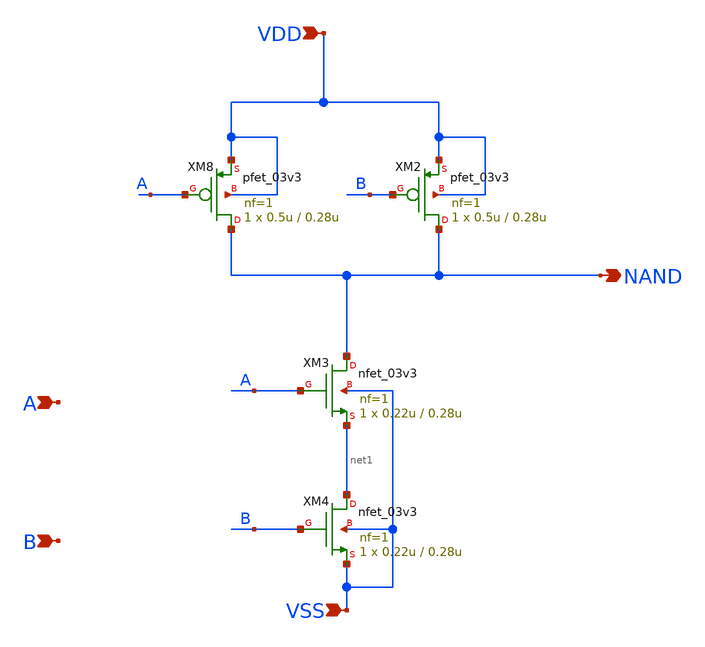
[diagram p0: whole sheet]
** sch_path: designs/libs/qw_core_analog_pkedit/NAND.sch
**.subckt NAND VDD VSS A B NAND
*.ipin VDD
*.ipin VSS
*.ipin A
*.ipin B
*.opin NAND
XM8 NAND A VDD VDD pfet_03v3 L=0.28u W=0.5u nf=1 ad='int((nf+1)/2) * W/nf * 0.18u' as='int((nf+2)/2) * W/nf * 0.18u'
+ pd='2*int((nf+1)/2) * (W/nf + 0.18u)' ps='2*int((nf+2)/2) * (W/nf + 0.18u)' nrd='0.18u / W' nrs='0.18u / W'
+ sa=0 sb=0 sd=0 m=1
XM2 NAND B VDD VDD pfet_03v3 L=0.28u W=0.5u nf=1 ad='int((nf+1)/2) * W/nf * 0.18u' as='int((nf+2)/2) * W/nf * 0.18u'
+ pd='2*int((nf+1)/2) * (W/nf + 0.18u)' ps='2*int((nf+2)/2) * (W/nf + 0.18u)' nrd='0.18u / W' nrs='0.18u / W'
+ sa=0 sb=0 sd=0 m=1
XM3 NAND A net1 VSS nfet_03v3 L=0.28u W=0.22u nf=1 ad='int((nf+1)/2) * W/nf * 0.18u' as='int((nf+2)/2) * W/nf * 0.18u'
+ pd='2*int((nf+1)/2) * (W/nf + 0.18u)' ps='2*int((nf+2)/2) * (W/nf + 0.18u)' nrd='0.18u / W' nrs='0.18u / W'
+ sa=0 sb=0 sd=0 m=1
XM4 net1 B VSS VSS nfet_03v3 L=0.28u W=0.22u nf=1 ad='int((nf+1)/2) * W/nf * 0.18u' as='int((nf+2)/2) * W/nf * 0.18u'
+ pd='2*int((nf+1)/2) * (W/nf + 0.18u)' ps='2*int((nf+2)/2) * (W/nf + 0.18u)' nrd='0.18u / W' nrs='0.18u / W'
+ sa=0 sb=0 sd=0 m=1
**.ends
.end
